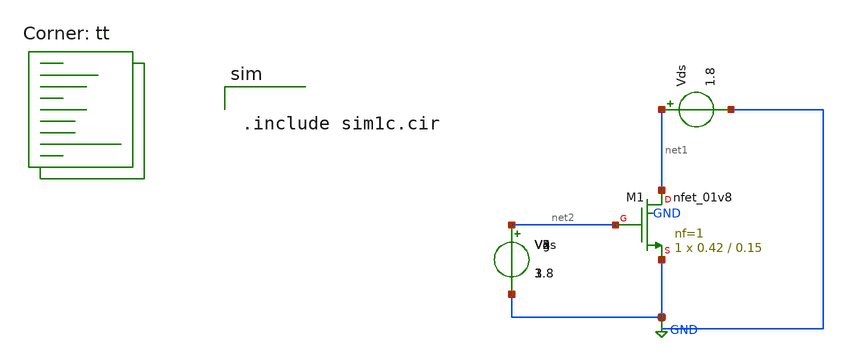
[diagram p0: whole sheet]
** sch_path: assignments/assignment1/assign1c.sch
**.subckt assign1c
XM1 net1 net2 GND GND sky130_fd_pr__nfet_01v8 L=0.15 W=0.42 nf=1 ad='int((nf+1)/2) * W/nf * 0.29' as='int((nf+2)/2) * W/nf * 0.29'
+ pd='2*int((nf+1)/2) * (W/nf + 0.29)' ps='2*int((nf+2)/2) * (W/nf + 0.29)' nrd='0.29 / W' nrs='0.29 / W'
+ sa=0 sb=0 sd=0 mult=1 m=1
Vgs net2 GND 1.8
V2 net2 GND 3
V3 net2 GND 3
V4 net2 GND 3
V5 net2 GND 3
Vds net1 GND 1.8
**** begin user architecture code


.include sim1c.cir


.lib $::SKYWATER_MODELS/sky130.lib.spice tt
**** end user architecture code
**.ends
.GLOBAL GND
.end
